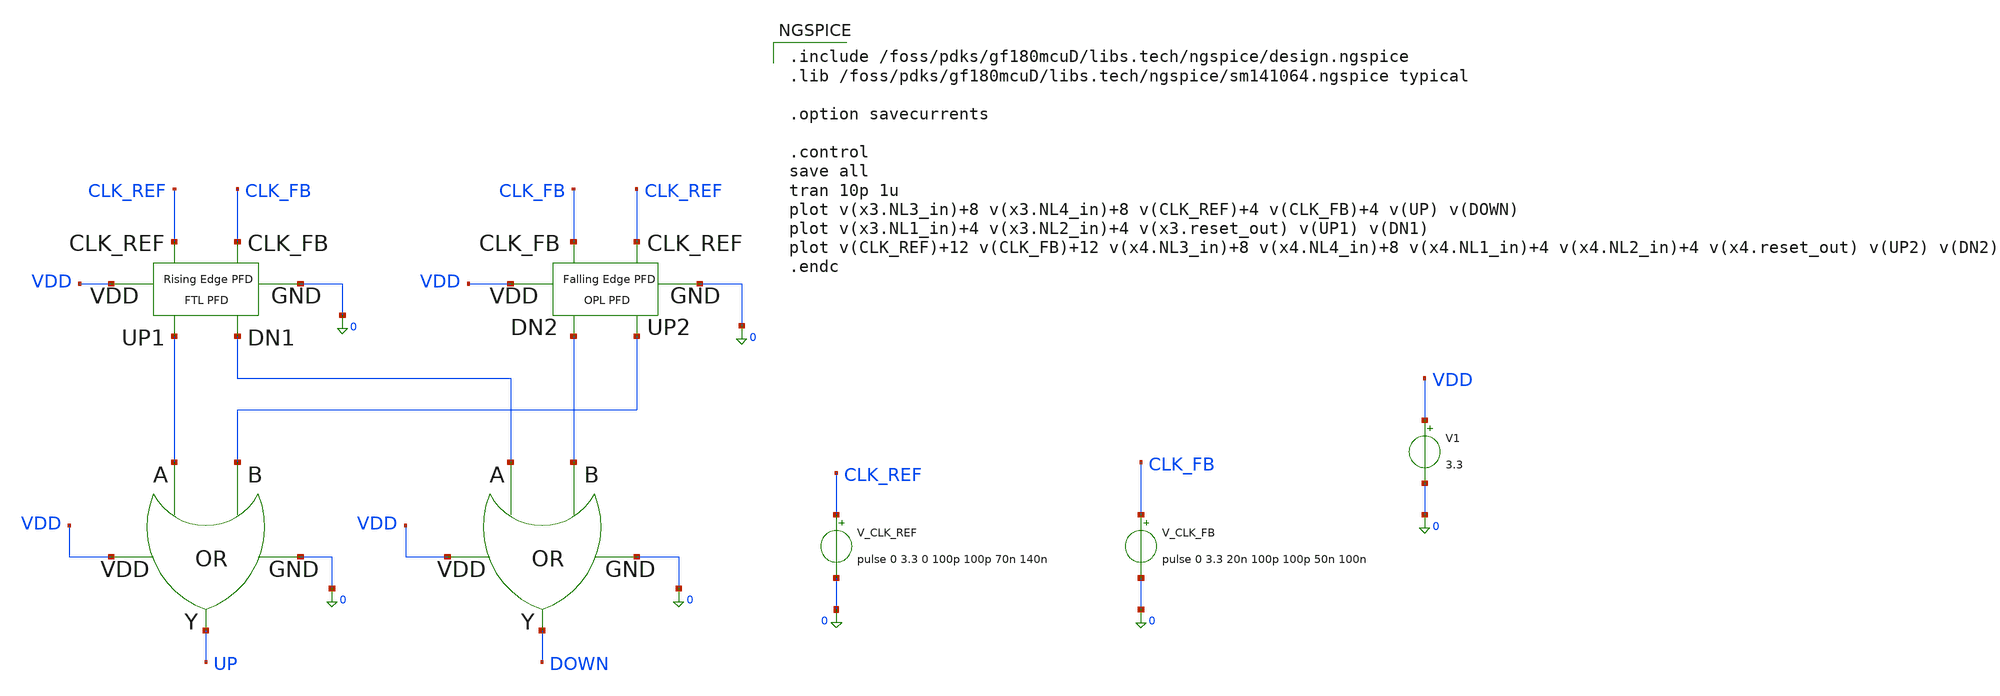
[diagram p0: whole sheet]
** sch_path: PFD/DELD_PFD.sch
**.subckt DELD_PFD
x1 0 DN1 DN2 VDD DOWN OR
x2 0 UP1 UP2 VDD UP OR
x3 DN1 UP1 CLK_FB CLK_REF VDD 0 FTL_PFD
x4 UP2 DN2 CLK_REF CLK_FB VDD 0 OPL_PFD
V1 VDD 0 3.3
.save i(v1)
V_CLK_REF CLK_REF 0 pulse 0 3.3 0 100p 100p 70n 140n
.save i(v_clk_ref)
V_CLK_FB CLK_FB 0 pulse 0 3.3 20n 100p 100p 50n 100n
.save i(v_clk_fb)
**** begin user architecture code

.include /foss/pdks/gf180mcuD/libs.tech/ngspice/design.ngspice
.lib /foss/pdks/gf180mcuD/libs.tech/ngspice/sm141064.ngspice typical

.option savecurrents

.control
save all
tran 10p 1u
plot v(x3.NL3_in)+8 v(x3.NL4_in)+8 v(CLK_REF)+4 v(CLK_FB)+4 v(UP) v(DOWN)
plot v(x3.NL1_in)+4 v(x3.NL2_in)+4 v(x3.reset_out) v(UP1) v(DN1)
plot v(CLK_REF)+12 v(CLK_FB)+12 v(x4.NL3_in)+8 v(x4.NL4_in)+8 v(x4.NL1_in)+4 v(x4.NL2_in)+4
+ v(x4.reset_out) v(UP2) v(DN2)
.endc

**** end user architecture code
**.ends

* expanding   symbol:  OR.sym # of pins=5
** sym_path: PFD/OR.sym
** sch_path: PFD/OR.sch
.subckt OR GND A B VDD Y
*.opin Y
*.ipin GND
*.ipin VDD
*.ipin A
*.ipin B
XM3 net2 A GND GND nfet_03v3 L=0.28u W=0.22u nf=1 ad='int((nf+1)/2) * W/nf * 0.18u' as='int((nf+2)/2) * W/nf * 0.18u'
+ pd='2*int((nf+1)/2) * (W/nf + 0.18u)' ps='2*int((nf+2)/2) * (W/nf + 0.18u)' nrd='0.18u / W' nrs='0.18u / W'
+ sa=0 sb=0 sd=0 m=1
XM2 net1 A net3 VDD pfet_03v3 L=0.28u W=0.22u nf=1 ad='int((nf+1)/2) * W/nf * 0.18u' as='int((nf+2)/2) * W/nf * 0.18u'
+ pd='2*int((nf+1)/2) * (W/nf + 0.18u)' ps='2*int((nf+2)/2) * (W/nf + 0.18u)' nrd='0.18u / W' nrs='0.18u / W'
+ sa=0 sb=0 sd=0 m=3
XM4 net2 B net1 net4 pfet_03v3 L=0.28u W=0.22u nf=1 ad='int((nf+1)/2) * W/nf * 0.18u' as='int((nf+2)/2) * W/nf * 0.18u'
+ pd='2*int((nf+1)/2) * (W/nf + 0.18u)' ps='2*int((nf+2)/2) * (W/nf + 0.18u)' nrd='0.18u / W' nrs='0.18u / W'
+ sa=0 sb=0 sd=0 m=3
XM1 net2 B GND GND nfet_03v3 L=0.28u W=0.22u nf=1 ad='int((nf+1)/2) * W/nf * 0.18u' as='int((nf+2)/2) * W/nf * 0.18u'
+ pd='2*int((nf+1)/2) * (W/nf + 0.18u)' ps='2*int((nf+2)/2) * (W/nf + 0.18u)' nrd='0.18u / W' nrs='0.18u / W'
+ sa=0 sb=0 sd=0 m=1
XM29 Y net2 VDD VDD pfet_03v3 L=0.28u W=0.22u nf=1 ad='int((nf+1)/2) * W/nf * 0.18u' as='int((nf+2)/2) * W/nf * 0.18u'
+ pd='2*int((nf+1)/2) * (W/nf + 0.18u)' ps='2*int((nf+2)/2) * (W/nf + 0.18u)' nrd='0.18u / W' nrs='0.18u / W'
+ sa=0 sb=0 sd=0 m=3
XM30 Y net2 GND GND nfet_03v3 L=0.28u W=0.22u nf=1 ad='int((nf+1)/2) * W/nf * 0.18u' as='int((nf+2)/2) * W/nf * 0.18u'
+ pd='2*int((nf+1)/2) * (W/nf + 0.18u)' ps='2*int((nf+2)/2) * (W/nf + 0.18u)' nrd='0.18u / W' nrs='0.18u / W'
+ sa=0 sb=0 sd=0 m=1
.ends


* expanding   symbol:  FTL_PFD.sym # of pins=6
** sym_path: PFD/FTL_PFD.sym
** sch_path: PFD/FTL_PFD.sch
.subckt FTL_PFD DN1 UP1 CLK_FB CLK_REF VDD GND
*.opin UP1
*.opin DN1
*.ipin CLK_FB
*.ipin CLK_REF
*.iopin VDD
*.iopin GND
XM1 net1 net3 VDD VDD pfet_03v3 L=0.28u W=0.22u nf=1 ad='int((nf+1)/2) * W/nf * 0.18u' as='int((nf+2)/2) * W/nf * 0.18u'
+ pd='2*int((nf+1)/2) * (W/nf + 0.18u)' ps='2*int((nf+2)/2) * (W/nf + 0.18u)' nrd='0.18u / W' nrs='0.18u / W'
+ sa=0 sb=0 sd=0 m=3
XM4 net2 net3 GND GND nfet_03v3 L=0.28u W=0.22u nf=1 ad='int((nf+1)/2) * W/nf * 0.18u' as='int((nf+2)/2) * W/nf * 0.18u'
+ pd='2*int((nf+1)/2) * (W/nf + 0.18u)' ps='2*int((nf+2)/2) * (W/nf + 0.18u)' nrd='0.18u / W' nrs='0.18u / W'
+ sa=0 sb=0 sd=0 m=1
XM2 net2 CLK_REF net1 VDD pfet_03v3 L=0.28u W=0.22u nf=1 ad='int((nf+1)/2) * W/nf * 0.18u' as='int((nf+2)/2) * W/nf * 0.18u'
+ pd='2*int((nf+1)/2) * (W/nf + 0.18u)' ps='2*int((nf+2)/2) * (W/nf + 0.18u)' nrd='0.18u / W' nrs='0.18u / W'
+ sa=0 sb=0 sd=0 m=3
XM3 net2 CLK_REF GND GND nfet_03v3 L=0.28u W=0.22u nf=1 ad='int((nf+1)/2) * W/nf * 0.18u' as='int((nf+2)/2) * W/nf * 0.18u'
+ pd='2*int((nf+1)/2) * (W/nf + 0.18u)' ps='2*int((nf+2)/2) * (W/nf + 0.18u)' nrd='0.18u / W' nrs='0.18u / W'
+ sa=0 sb=0 sd=0 m=1
XM5 net4 net2 VDD VDD pfet_03v3 L=0.28u W=0.22u nf=1 ad='int((nf+1)/2) * W/nf * 0.18u' as='int((nf+2)/2) * W/nf * 0.18u'
+ pd='2*int((nf+1)/2) * (W/nf + 0.18u)' ps='2*int((nf+2)/2) * (W/nf + 0.18u)' nrd='0.18u / W' nrs='0.18u / W'
+ sa=0 sb=0 sd=0 m=3
XM6 net5 CLK_REF net4 VDD pfet_03v3 L=0.28u W=0.22u nf=1 ad='int((nf+1)/2) * W/nf * 0.18u' as='int((nf+2)/2) * W/nf * 0.18u'
+ pd='2*int((nf+1)/2) * (W/nf + 0.18u)' ps='2*int((nf+2)/2) * (W/nf + 0.18u)' nrd='0.18u / W' nrs='0.18u / W'
+ sa=0 sb=0 sd=0 m=3
XM7 net5 net2 GND GND nfet_03v3 L=0.28u W=0.22u nf=1 ad='int((nf+1)/2) * W/nf * 0.18u' as='int((nf+2)/2) * W/nf * 0.18u'
+ pd='2*int((nf+1)/2) * (W/nf + 0.18u)' ps='2*int((nf+2)/2) * (W/nf + 0.18u)' nrd='0.18u / W' nrs='0.18u / W'
+ sa=0 sb=0 sd=0 m=1
XM9 net6 CLK_REF_bar VDD VDD pfet_03v3 L=0.28u W=0.22u nf=1 ad='int((nf+1)/2) * W/nf * 0.18u' as='int((nf+2)/2) * W/nf * 0.18u'
+ pd='2*int((nf+1)/2) * (W/nf + 0.18u)' ps='2*int((nf+2)/2) * (W/nf + 0.18u)' nrd='0.18u / W' nrs='0.18u / W'
+ sa=0 sb=0 sd=0 m=3
XM10 net7 net5 GND GND nfet_03v3 L=0.28u W=0.22u nf=1 ad='int((nf+1)/2) * W/nf * 0.18u' as='int((nf+2)/2) * W/nf * 0.18u'
+ pd='2*int((nf+1)/2) * (W/nf + 0.18u)' ps='2*int((nf+2)/2) * (W/nf + 0.18u)' nrd='0.18u / W' nrs='0.18u / W'
+ sa=0 sb=0 sd=0 m=1
XM8 net7 net5 net6 VDD pfet_03v3 L=0.28u W=0.22u nf=1 ad='int((nf+1)/2) * W/nf * 0.18u' as='int((nf+2)/2) * W/nf * 0.18u'
+ pd='2*int((nf+1)/2) * (W/nf + 0.18u)' ps='2*int((nf+2)/2) * (W/nf + 0.18u)' nrd='0.18u / W' nrs='0.18u / W'
+ sa=0 sb=0 sd=0 m=3
XM11 net7 CLK_REF_bar GND GND nfet_03v3 L=0.28u W=0.22u nf=1 ad='int((nf+1)/2) * W/nf * 0.18u' as='int((nf+2)/2) * W/nf * 0.18u'
+ pd='2*int((nf+1)/2) * (W/nf + 0.18u)' ps='2*int((nf+2)/2) * (W/nf + 0.18u)' nrd='0.18u / W' nrs='0.18u / W'
+ sa=0 sb=0 sd=0 m=1
XM12 net8 net7 VDD VDD pfet_03v3 L=0.28u W=0.22u nf=1 ad='int((nf+1)/2) * W/nf * 0.18u' as='int((nf+2)/2) * W/nf * 0.18u'
+ pd='2*int((nf+1)/2) * (W/nf + 0.18u)' ps='2*int((nf+2)/2) * (W/nf + 0.18u)' nrd='0.18u / W' nrs='0.18u / W'
+ sa=0 sb=0 sd=0 m=3
XM13 UP1 CLK_REF_bar net8 VDD pfet_03v3 L=0.28u W=0.22u nf=1 ad='int((nf+1)/2) * W/nf * 0.18u' as='int((nf+2)/2) * W/nf * 0.18u'
+ pd='2*int((nf+1)/2) * (W/nf + 0.18u)' ps='2*int((nf+2)/2) * (W/nf + 0.18u)' nrd='0.18u / W' nrs='0.18u / W'
+ sa=0 sb=0 sd=0 m=3
XM14 UP1 net7 GND GND nfet_03v3 L=0.28u W=0.22u nf=1 ad='int((nf+1)/2) * W/nf * 0.18u' as='int((nf+2)/2) * W/nf * 0.18u'
+ pd='2*int((nf+1)/2) * (W/nf + 0.18u)' ps='2*int((nf+2)/2) * (W/nf + 0.18u)' nrd='0.18u / W' nrs='0.18u / W'
+ sa=0 sb=0 sd=0 m=1
XM15 net9 net3 VDD VDD pfet_03v3 L=0.28u W=0.22u nf=1 ad='int((nf+1)/2) * W/nf * 0.18u' as='int((nf+2)/2) * W/nf * 0.18u'
+ pd='2*int((nf+1)/2) * (W/nf + 0.18u)' ps='2*int((nf+2)/2) * (W/nf + 0.18u)' nrd='0.18u / W' nrs='0.18u / W'
+ sa=0 sb=0 sd=0 m=3
XM16 net10 net3 GND GND nfet_03v3 L=0.28u W=0.22u nf=1 ad='int((nf+1)/2) * W/nf * 0.18u' as='int((nf+2)/2) * W/nf * 0.18u'
+ pd='2*int((nf+1)/2) * (W/nf + 0.18u)' ps='2*int((nf+2)/2) * (W/nf + 0.18u)' nrd='0.18u / W' nrs='0.18u / W'
+ sa=0 sb=0 sd=0 m=1
XM17 net10 CLK_FB net9 VDD pfet_03v3 L=0.28u W=0.22u nf=1 ad='int((nf+1)/2) * W/nf * 0.18u' as='int((nf+2)/2) * W/nf * 0.18u'
+ pd='2*int((nf+1)/2) * (W/nf + 0.18u)' ps='2*int((nf+2)/2) * (W/nf + 0.18u)' nrd='0.18u / W' nrs='0.18u / W'
+ sa=0 sb=0 sd=0 m=3
XM18 net10 CLK_FB GND GND nfet_03v3 L=0.28u W=0.22u nf=1 ad='int((nf+1)/2) * W/nf * 0.18u' as='int((nf+2)/2) * W/nf * 0.18u'
+ pd='2*int((nf+1)/2) * (W/nf + 0.18u)' ps='2*int((nf+2)/2) * (W/nf + 0.18u)' nrd='0.18u / W' nrs='0.18u / W'
+ sa=0 sb=0 sd=0 m=1
XM19 net11 net10 VDD VDD pfet_03v3 L=0.28u W=0.22u nf=1 ad='int((nf+1)/2) * W/nf * 0.18u' as='int((nf+2)/2) * W/nf * 0.18u'
+ pd='2*int((nf+1)/2) * (W/nf + 0.18u)' ps='2*int((nf+2)/2) * (W/nf + 0.18u)' nrd='0.18u / W' nrs='0.18u / W'
+ sa=0 sb=0 sd=0 m=3
XM20 net12 CLK_FB net11 VDD pfet_03v3 L=0.28u W=0.22u nf=1 ad='int((nf+1)/2) * W/nf * 0.18u' as='int((nf+2)/2) * W/nf * 0.18u'
+ pd='2*int((nf+1)/2) * (W/nf + 0.18u)' ps='2*int((nf+2)/2) * (W/nf + 0.18u)' nrd='0.18u / W' nrs='0.18u / W'
+ sa=0 sb=0 sd=0 m=3
XM21 net12 net10 GND GND nfet_03v3 L=0.28u W=0.22u nf=1 ad='int((nf+1)/2) * W/nf * 0.18u' as='int((nf+2)/2) * W/nf * 0.18u'
+ pd='2*int((nf+1)/2) * (W/nf + 0.18u)' ps='2*int((nf+2)/2) * (W/nf + 0.18u)' nrd='0.18u / W' nrs='0.18u / W'
+ sa=0 sb=0 sd=0 m=1
XM22 net13 CLK_FB_bar VDD VDD pfet_03v3 L=0.28u W=0.22u nf=1 ad='int((nf+1)/2) * W/nf * 0.18u' as='int((nf+2)/2) * W/nf * 0.18u'
+ pd='2*int((nf+1)/2) * (W/nf + 0.18u)' ps='2*int((nf+2)/2) * (W/nf + 0.18u)' nrd='0.18u / W' nrs='0.18u / W'
+ sa=0 sb=0 sd=0 m=3
XM23 net14 net12 GND GND nfet_03v3 L=0.28u W=0.22u nf=1 ad='int((nf+1)/2) * W/nf * 0.18u' as='int((nf+2)/2) * W/nf * 0.18u'
+ pd='2*int((nf+1)/2) * (W/nf + 0.18u)' ps='2*int((nf+2)/2) * (W/nf + 0.18u)' nrd='0.18u / W' nrs='0.18u / W'
+ sa=0 sb=0 sd=0 m=1
XM24 net14 net12 net13 VDD pfet_03v3 L=0.28u W=0.22u nf=1 ad='int((nf+1)/2) * W/nf * 0.18u' as='int((nf+2)/2) * W/nf * 0.18u'
+ pd='2*int((nf+1)/2) * (W/nf + 0.18u)' ps='2*int((nf+2)/2) * (W/nf + 0.18u)' nrd='0.18u / W' nrs='0.18u / W'
+ sa=0 sb=0 sd=0 m=3
XM25 net14 CLK_FB_bar GND GND nfet_03v3 L=0.28u W=0.22u nf=1 ad='int((nf+1)/2) * W/nf * 0.18u' as='int((nf+2)/2) * W/nf * 0.18u'
+ pd='2*int((nf+1)/2) * (W/nf + 0.18u)' ps='2*int((nf+2)/2) * (W/nf + 0.18u)' nrd='0.18u / W' nrs='0.18u / W'
+ sa=0 sb=0 sd=0 m=1
XM26 net15 net14 VDD VDD pfet_03v3 L=0.28u W=0.22u nf=1 ad='int((nf+1)/2) * W/nf * 0.18u' as='int((nf+2)/2) * W/nf * 0.18u'
+ pd='2*int((nf+1)/2) * (W/nf + 0.18u)' ps='2*int((nf+2)/2) * (W/nf + 0.18u)' nrd='0.18u / W' nrs='0.18u / W'
+ sa=0 sb=0 sd=0 m=3
XM27 DN1 CLK_FB_bar net15 VDD pfet_03v3 L=0.28u W=0.22u nf=1 ad='int((nf+1)/2) * W/nf * 0.18u' as='int((nf+2)/2) * W/nf * 0.18u'
+ pd='2*int((nf+1)/2) * (W/nf + 0.18u)' ps='2*int((nf+2)/2) * (W/nf + 0.18u)' nrd='0.18u / W' nrs='0.18u / W'
+ sa=0 sb=0 sd=0 m=3
XM28 DN1 net14 GND GND nfet_03v3 L=0.28u W=0.22u nf=1 ad='int((nf+1)/2) * W/nf * 0.18u' as='int((nf+2)/2) * W/nf * 0.18u'
+ pd='2*int((nf+1)/2) * (W/nf + 0.18u)' ps='2*int((nf+2)/2) * (W/nf + 0.18u)' nrd='0.18u / W' nrs='0.18u / W'
+ sa=0 sb=0 sd=0 m=1
x1 GND UP1 DN1 VDD net3 XNOR
XM29 CLK_FB_bar CLK_FB VDD VDD pfet_03v3 L=0.28u W=0.22u nf=1 ad='int((nf+1)/2) * W/nf * 0.18u' as='int((nf+2)/2) * W/nf * 0.18u'
+ pd='2*int((nf+1)/2) * (W/nf + 0.18u)' ps='2*int((nf+2)/2) * (W/nf + 0.18u)' nrd='0.18u / W' nrs='0.18u / W'
+ sa=0 sb=0 sd=0 m=3
XM30 CLK_FB_bar CLK_FB GND GND nfet_03v3 L=0.28u W=0.22u nf=1 ad='int((nf+1)/2) * W/nf * 0.18u' as='int((nf+2)/2) * W/nf * 0.18u'
+ pd='2*int((nf+1)/2) * (W/nf + 0.18u)' ps='2*int((nf+2)/2) * (W/nf + 0.18u)' nrd='0.18u / W' nrs='0.18u / W'
+ sa=0 sb=0 sd=0 m=1
XM31 CLK_REF_bar CLK_REF VDD VDD pfet_03v3 L=0.28u W=0.22u nf=1 ad='int((nf+1)/2) * W/nf * 0.18u' as='int((nf+2)/2) * W/nf * 0.18u'
+ pd='2*int((nf+1)/2) * (W/nf + 0.18u)' ps='2*int((nf+2)/2) * (W/nf + 0.18u)' nrd='0.18u / W' nrs='0.18u / W'
+ sa=0 sb=0 sd=0 m=3
XM32 CLK_REF_bar CLK_REF GND GND nfet_03v3 L=0.28u W=0.22u nf=1 ad='int((nf+1)/2) * W/nf * 0.18u' as='int((nf+2)/2) * W/nf * 0.18u'
+ pd='2*int((nf+1)/2) * (W/nf + 0.18u)' ps='2*int((nf+2)/2) * (W/nf + 0.18u)' nrd='0.18u / W' nrs='0.18u / W'
+ sa=0 sb=0 sd=0 m=1
.ends


* expanding   symbol:  OPL_PFD.sym # of pins=6
** sym_path: PFD/OPL_PFD.sym
** sch_path: PFD/OPL_PFD.sch
.subckt OPL_PFD UP2 DN2 CLK_REF CLK_FB VDD GND
*.opin UP2
*.ipin CLK_FB
*.ipin CLK_REF
*.opin DN2
*.iopin VDD
*.iopin GND
XM1 NL1_in reset_out VDD VDD pfet_03v3 L=0.28u W=0.22u nf=1 ad='int((nf+1)/2) * W/nf * 0.18u' as='int((nf+2)/2) * W/nf * 0.18u'
+ pd='2*int((nf+1)/2) * (W/nf + 0.18u)' ps='2*int((nf+2)/2) * (W/nf + 0.18u)' nrd='0.18u / W' nrs='0.18u / W'
+ sa=0 sb=0 sd=0 m=3
XM4 net1 reset_out GND GND nfet_03v3 L=0.28u W=0.22u nf=1 ad='int((nf+1)/2) * W/nf * 0.18u' as='int((nf+2)/2) * W/nf * 0.18u'
+ pd='2*int((nf+1)/2) * (W/nf + 0.18u)' ps='2*int((nf+2)/2) * (W/nf + 0.18u)' nrd='0.18u / W' nrs='0.18u / W'
+ sa=0 sb=0 sd=0 m=1
XM5 net2 NL1_in VDD VDD pfet_03v3 L=0.28u W=0.22u nf=1 ad='int((nf+1)/2) * W/nf * 0.18u' as='int((nf+2)/2) * W/nf * 0.18u'
+ pd='2*int((nf+1)/2) * (W/nf + 0.18u)' ps='2*int((nf+2)/2) * (W/nf + 0.18u)' nrd='0.18u / W' nrs='0.18u / W'
+ sa=0 sb=0 sd=0 m=3
XM7 net3 NL1_in GND GND nfet_03v3 L=0.28u W=0.22u nf=1 ad='int((nf+1)/2) * W/nf * 0.18u' as='int((nf+2)/2) * W/nf * 0.18u'
+ pd='2*int((nf+1)/2) * (W/nf + 0.18u)' ps='2*int((nf+2)/2) * (W/nf + 0.18u)' nrd='0.18u / W' nrs='0.18u / W'
+ sa=0 sb=0 sd=0 m=1
XM9 NL2_in CLK_REF_bar VDD VDD pfet_03v3 L=0.28u W=0.22u nf=1 ad='int((nf+1)/2) * W/nf * 0.18u' as='int((nf+2)/2) * W/nf * 0.18u'
+ pd='2*int((nf+1)/2) * (W/nf + 0.18u)' ps='2*int((nf+2)/2) * (W/nf + 0.18u)' nrd='0.18u / W' nrs='0.18u / W'
+ sa=0 sb=0 sd=0 m=3
XM11 net8 CLK_REF_bar GND GND nfet_03v3 L=0.28u W=0.22u nf=1 ad='int((nf+1)/2) * W/nf * 0.18u' as='int((nf+2)/2) * W/nf * 0.18u'
+ pd='2*int((nf+1)/2) * (W/nf + 0.18u)' ps='2*int((nf+2)/2) * (W/nf + 0.18u)' nrd='0.18u / W' nrs='0.18u / W'
+ sa=0 sb=0 sd=0 m=1
XM12 net7 NL2_in VDD VDD pfet_03v3 L=0.28u W=0.22u nf=1 ad='int((nf+1)/2) * W/nf * 0.18u' as='int((nf+2)/2) * W/nf * 0.18u'
+ pd='2*int((nf+1)/2) * (W/nf + 0.18u)' ps='2*int((nf+2)/2) * (W/nf + 0.18u)' nrd='0.18u / W' nrs='0.18u / W'
+ sa=0 sb=0 sd=0 m=1
XM14 net9 NL2_in GND GND nfet_03v3 L=0.28u W=0.22u nf=1 ad='int((nf+1)/2) * W/nf * 0.18u' as='int((nf+2)/2) * W/nf * 0.18u'
+ pd='2*int((nf+1)/2) * (W/nf + 0.18u)' ps='2*int((nf+2)/2) * (W/nf + 0.18u)' nrd='0.18u / W' nrs='0.18u / W'
+ sa=0 sb=0 sd=0 m=1
XM2 NL1_in CLK_REF VDD VDD pfet_03v3 L=0.28u W=0.22u nf=1 ad='int((nf+1)/2) * W/nf * 0.18u' as='int((nf+2)/2) * W/nf * 0.18u'
+ pd='2*int((nf+1)/2) * (W/nf + 0.18u)' ps='2*int((nf+2)/2) * (W/nf + 0.18u)' nrd='0.18u / W' nrs='0.18u / W'
+ sa=0 sb=0 sd=0 m=3
XM6 net2 CLK_REF net3 GND nfet_03v3 L=0.28u W=0.22u nf=1 ad='int((nf+1)/2) * W/nf * 0.18u' as='int((nf+2)/2) * W/nf * 0.18u'
+ pd='2*int((nf+1)/2) * (W/nf + 0.18u)' ps='2*int((nf+2)/2) * (W/nf + 0.18u)' nrd='0.18u / W' nrs='0.18u / W'
+ sa=0 sb=0 sd=0 m=1
XM10 NL2_in net2 net8 GND nfet_03v3 L=0.28u W=0.22u nf=1 ad='int((nf+1)/2) * W/nf * 0.18u' as='int((nf+2)/2) * W/nf * 0.18u'
+ pd='2*int((nf+1)/2) * (W/nf + 0.18u)' ps='2*int((nf+2)/2) * (W/nf + 0.18u)' nrd='0.18u / W' nrs='0.18u / W'
+ sa=0 sb=0 sd=0 m=1
XM8 NL2_in net2 VDD VDD pfet_03v3 L=0.28u W=0.22u nf=1 ad='int((nf+1)/2) * W/nf * 0.18u' as='int((nf+2)/2) * W/nf * 0.18u'
+ pd='2*int((nf+1)/2) * (W/nf + 0.18u)' ps='2*int((nf+2)/2) * (W/nf + 0.18u)' nrd='0.18u / W' nrs='0.18u / W'
+ sa=0 sb=0 sd=0 m=3
XM13 net7 CLK_REF_bar net9 GND nfet_03v3 L=0.28u W=0.22u nf=1 ad='int((nf+1)/2) * W/nf * 0.18u' as='int((nf+2)/2) * W/nf * 0.18u'
+ pd='2*int((nf+1)/2) * (W/nf + 0.18u)' ps='2*int((nf+2)/2) * (W/nf + 0.18u)' nrd='0.18u / W' nrs='0.18u / W'
+ sa=0 sb=0 sd=0 m=1
XM15 UP2 net7 VDD VDD pfet_03v3 L=0.28u W=0.22u nf=1 ad='int((nf+1)/2) * W/nf * 0.18u' as='int((nf+2)/2) * W/nf * 0.18u'
+ pd='2*int((nf+1)/2) * (W/nf + 0.18u)' ps='2*int((nf+2)/2) * (W/nf + 0.18u)' nrd='0.18u / W' nrs='0.18u / W'
+ sa=0 sb=0 sd=0 m=3
XM16 UP2 net7 GND GND nfet_03v3 L=0.28u W=0.22u nf=1 ad='int((nf+1)/2) * W/nf * 0.18u' as='int((nf+2)/2) * W/nf * 0.18u'
+ pd='2*int((nf+1)/2) * (W/nf + 0.18u)' ps='2*int((nf+2)/2) * (W/nf + 0.18u)' nrd='0.18u / W' nrs='0.18u / W'
+ sa=0 sb=0 sd=0 m=1
XM17 CLK_FB_bar CLK_FB VDD VDD pfet_03v3 L=0.28u W=0.22u nf=1 ad='int((nf+1)/2) * W/nf * 0.18u' as='int((nf+2)/2) * W/nf * 0.18u'
+ pd='2*int((nf+1)/2) * (W/nf + 0.18u)' ps='2*int((nf+2)/2) * (W/nf + 0.18u)' nrd='0.18u / W' nrs='0.18u / W'
+ sa=0 sb=0 sd=0 m=3
XM18 CLK_FB_bar CLK_FB GND GND nfet_03v3 L=0.28u W=0.22u nf=1 ad='int((nf+1)/2) * W/nf * 0.18u' as='int((nf+2)/2) * W/nf * 0.18u'
+ pd='2*int((nf+1)/2) * (W/nf + 0.18u)' ps='2*int((nf+2)/2) * (W/nf + 0.18u)' nrd='0.18u / W' nrs='0.18u / W'
+ sa=0 sb=0 sd=0 m=1
XM19 CLK_REF_bar CLK_REF VDD VDD pfet_03v3 L=0.28u W=0.22u nf=1 ad='int((nf+1)/2) * W/nf * 0.18u' as='int((nf+2)/2) * W/nf * 0.18u'
+ pd='2*int((nf+1)/2) * (W/nf + 0.18u)' ps='2*int((nf+2)/2) * (W/nf + 0.18u)' nrd='0.18u / W' nrs='0.18u / W'
+ sa=0 sb=0 sd=0 m=3
XM20 CLK_REF_bar CLK_REF GND GND nfet_03v3 L=0.28u W=0.22u nf=1 ad='int((nf+1)/2) * W/nf * 0.18u' as='int((nf+2)/2) * W/nf * 0.18u'
+ pd='2*int((nf+1)/2) * (W/nf + 0.18u)' ps='2*int((nf+2)/2) * (W/nf + 0.18u)' nrd='0.18u / W' nrs='0.18u / W'
+ sa=0 sb=0 sd=0 m=1
XM3 NL1_in CLK_REF net1 GND nfet_03v3 L=0.28u W=0.22u nf=1 ad='int((nf+1)/2) * W/nf * 0.18u' as='int((nf+2)/2) * W/nf * 0.18u'
+ pd='2*int((nf+1)/2) * (W/nf + 0.18u)' ps='2*int((nf+2)/2) * (W/nf + 0.18u)' nrd='0.18u / W' nrs='0.18u / W'
+ sa=0 sb=0 sd=0 m=1
XM21 NL3_in reset_out VDD VDD pfet_03v3 L=0.28u W=0.22u nf=1 ad='int((nf+1)/2) * W/nf * 0.18u' as='int((nf+2)/2) * W/nf * 0.18u'
+ pd='2*int((nf+1)/2) * (W/nf + 0.18u)' ps='2*int((nf+2)/2) * (W/nf + 0.18u)' nrd='0.18u / W' nrs='0.18u / W'
+ sa=0 sb=0 sd=0 m=3
XM22 net10 reset_out GND GND nfet_03v3 L=0.28u W=0.22u nf=1 ad='int((nf+1)/2) * W/nf * 0.18u' as='int((nf+2)/2) * W/nf * 0.18u'
+ pd='2*int((nf+1)/2) * (W/nf + 0.18u)' ps='2*int((nf+2)/2) * (W/nf + 0.18u)' nrd='0.18u / W' nrs='0.18u / W'
+ sa=0 sb=0 sd=0 m=1
XM23 net6 NL3_in VDD VDD pfet_03v3 L=0.28u W=0.22u nf=1 ad='int((nf+1)/2) * W/nf * 0.18u' as='int((nf+2)/2) * W/nf * 0.18u'
+ pd='2*int((nf+1)/2) * (W/nf + 0.18u)' ps='2*int((nf+2)/2) * (W/nf + 0.18u)' nrd='0.18u / W' nrs='0.18u / W'
+ sa=0 sb=0 sd=0 m=3
XM24 net11 NL3_in GND GND nfet_03v3 L=0.28u W=0.22u nf=1 ad='int((nf+1)/2) * W/nf * 0.18u' as='int((nf+2)/2) * W/nf * 0.18u'
+ pd='2*int((nf+1)/2) * (W/nf + 0.18u)' ps='2*int((nf+2)/2) * (W/nf + 0.18u)' nrd='0.18u / W' nrs='0.18u / W'
+ sa=0 sb=0 sd=0 m=1
XM25 NL4_in CLK_FB_bar VDD VDD pfet_03v3 L=0.28u W=0.22u nf=1 ad='int((nf+1)/2) * W/nf * 0.18u' as='int((nf+2)/2) * W/nf * 0.18u'
+ pd='2*int((nf+1)/2) * (W/nf + 0.18u)' ps='2*int((nf+2)/2) * (W/nf + 0.18u)' nrd='0.18u / W' nrs='0.18u / W'
+ sa=0 sb=0 sd=0 m=3
XM26 net4 CLK_FB_bar GND GND nfet_03v3 L=0.28u W=0.22u nf=1 ad='int((nf+1)/2) * W/nf * 0.18u' as='int((nf+2)/2) * W/nf * 0.18u'
+ pd='2*int((nf+1)/2) * (W/nf + 0.18u)' ps='2*int((nf+2)/2) * (W/nf + 0.18u)' nrd='0.18u / W' nrs='0.18u / W'
+ sa=0 sb=0 sd=0 m=1
XM27 net5 NL4_in VDD VDD pfet_03v3 L=0.28u W=0.22u nf=1 ad='int((nf+1)/2) * W/nf * 0.18u' as='int((nf+2)/2) * W/nf * 0.18u'
+ pd='2*int((nf+1)/2) * (W/nf + 0.18u)' ps='2*int((nf+2)/2) * (W/nf + 0.18u)' nrd='0.18u / W' nrs='0.18u / W'
+ sa=0 sb=0 sd=0 m=1
XM28 net12 NL4_in GND GND nfet_03v3 L=0.28u W=0.22u nf=1 ad='int((nf+1)/2) * W/nf * 0.18u' as='int((nf+2)/2) * W/nf * 0.18u'
+ pd='2*int((nf+1)/2) * (W/nf + 0.18u)' ps='2*int((nf+2)/2) * (W/nf + 0.18u)' nrd='0.18u / W' nrs='0.18u / W'
+ sa=0 sb=0 sd=0 m=1
XM29 NL3_in CLK_FB VDD VDD pfet_03v3 L=0.28u W=0.22u nf=1 ad='int((nf+1)/2) * W/nf * 0.18u' as='int((nf+2)/2) * W/nf * 0.18u'
+ pd='2*int((nf+1)/2) * (W/nf + 0.18u)' ps='2*int((nf+2)/2) * (W/nf + 0.18u)' nrd='0.18u / W' nrs='0.18u / W'
+ sa=0 sb=0 sd=0 m=3
XM30 net6 CLK_FB net11 GND nfet_03v3 L=0.28u W=0.22u nf=1 ad='int((nf+1)/2) * W/nf * 0.18u' as='int((nf+2)/2) * W/nf * 0.18u'
+ pd='2*int((nf+1)/2) * (W/nf + 0.18u)' ps='2*int((nf+2)/2) * (W/nf + 0.18u)' nrd='0.18u / W' nrs='0.18u / W'
+ sa=0 sb=0 sd=0 m=1
XM31 NL4_in net6 net4 GND nfet_03v3 L=0.28u W=0.22u nf=1 ad='int((nf+1)/2) * W/nf * 0.18u' as='int((nf+2)/2) * W/nf * 0.18u'
+ pd='2*int((nf+1)/2) * (W/nf + 0.18u)' ps='2*int((nf+2)/2) * (W/nf + 0.18u)' nrd='0.18u / W' nrs='0.18u / W'
+ sa=0 sb=0 sd=0 m=1
XM32 NL4_in net6 VDD VDD pfet_03v3 L=0.28u W=0.22u nf=1 ad='int((nf+1)/2) * W/nf * 0.18u' as='int((nf+2)/2) * W/nf * 0.18u'
+ pd='2*int((nf+1)/2) * (W/nf + 0.18u)' ps='2*int((nf+2)/2) * (W/nf + 0.18u)' nrd='0.18u / W' nrs='0.18u / W'
+ sa=0 sb=0 sd=0 m=3
XM33 net5 CLK_FB_bar net12 GND nfet_03v3 L=0.28u W=0.22u nf=1 ad='int((nf+1)/2) * W/nf * 0.18u' as='int((nf+2)/2) * W/nf * 0.18u'
+ pd='2*int((nf+1)/2) * (W/nf + 0.18u)' ps='2*int((nf+2)/2) * (W/nf + 0.18u)' nrd='0.18u / W' nrs='0.18u / W'
+ sa=0 sb=0 sd=0 m=1
XM34 DN2 net5 VDD VDD pfet_03v3 L=0.28u W=0.22u nf=1 ad='int((nf+1)/2) * W/nf * 0.18u' as='int((nf+2)/2) * W/nf * 0.18u'
+ pd='2*int((nf+1)/2) * (W/nf + 0.18u)' ps='2*int((nf+2)/2) * (W/nf + 0.18u)' nrd='0.18u / W' nrs='0.18u / W'
+ sa=0 sb=0 sd=0 m=3
XM35 DN2 net5 GND GND nfet_03v3 L=0.28u W=0.22u nf=1 ad='int((nf+1)/2) * W/nf * 0.18u' as='int((nf+2)/2) * W/nf * 0.18u'
+ pd='2*int((nf+1)/2) * (W/nf + 0.18u)' ps='2*int((nf+2)/2) * (W/nf + 0.18u)' nrd='0.18u / W' nrs='0.18u / W'
+ sa=0 sb=0 sd=0 m=1
XM36 NL3_in CLK_FB net10 GND nfet_03v3 L=0.28u W=0.22u nf=1 ad='int((nf+1)/2) * W/nf * 0.18u' as='int((nf+2)/2) * W/nf * 0.18u'
+ pd='2*int((nf+1)/2) * (W/nf + 0.18u)' ps='2*int((nf+2)/2) * (W/nf + 0.18u)' nrd='0.18u / W' nrs='0.18u / W'
+ sa=0 sb=0 sd=0 m=1
x1 GND UP2 DN2 VDD reset_out NAND
.ends


* expanding   symbol:  XNOR.sym # of pins=5
** sym_path: PFD/XNOR.sym
** sch_path: PFD/XNOR.sch
.subckt XNOR GND A B VDD Y
*.opin Y
*.ipin A
*.ipin B
*.iopin VDD
*.iopin GND
XM1 net1 A VDD VDD pfet_03v3 L=0.28u W=0.22u nf=1 ad='int((nf+1)/2) * W/nf * 0.18u' as='int((nf+2)/2) * W/nf * 0.18u'
+ pd='2*int((nf+1)/2) * (W/nf + 0.18u)' ps='2*int((nf+2)/2) * (W/nf + 0.18u)' nrd='0.18u / W' nrs='0.18u / W'
+ sa=0 sb=0 sd=0 m=1
XM2 Y A_bar net1 VDD pfet_03v3 L=0.28u W=0.22u nf=1 ad='int((nf+1)/2) * W/nf * 0.18u' as='int((nf+2)/2) * W/nf * 0.18u'
+ pd='2*int((nf+1)/2) * (W/nf + 0.18u)' ps='2*int((nf+2)/2) * (W/nf + 0.18u)' nrd='0.18u / W' nrs='0.18u / W'
+ sa=0 sb=0 sd=0 m=1
XM3 Y B_bar net2 GND nfet_03v3 L=0.28u W=0.22u nf=1 ad='int((nf+1)/2) * W/nf * 0.18u' as='int((nf+2)/2) * W/nf * 0.18u'
+ pd='2*int((nf+1)/2) * (W/nf + 0.18u)' ps='2*int((nf+2)/2) * (W/nf + 0.18u)' nrd='0.18u / W' nrs='0.18u / W'
+ sa=0 sb=0 sd=0 m=1
XM4 net2 A GND GND nfet_03v3 L=0.28u W=0.22u nf=1 ad='int((nf+1)/2) * W/nf * 0.18u' as='int((nf+2)/2) * W/nf * 0.18u'
+ pd='2*int((nf+1)/2) * (W/nf + 0.18u)' ps='2*int((nf+2)/2) * (W/nf + 0.18u)' nrd='0.18u / W' nrs='0.18u / W'
+ sa=0 sb=0 sd=0 m=1
XM5 net3 B_bar VDD VDD pfet_03v3 L=0.28u W=0.22u nf=1 ad='int((nf+1)/2) * W/nf * 0.18u' as='int((nf+2)/2) * W/nf * 0.18u'
+ pd='2*int((nf+1)/2) * (W/nf + 0.18u)' ps='2*int((nf+2)/2) * (W/nf + 0.18u)' nrd='0.18u / W' nrs='0.18u / W'
+ sa=0 sb=0 sd=0 m=1
XM6 Y B net3 VDD pfet_03v3 L=0.28u W=0.22u nf=1 ad='int((nf+1)/2) * W/nf * 0.18u' as='int((nf+2)/2) * W/nf * 0.18u'
+ pd='2*int((nf+1)/2) * (W/nf + 0.18u)' ps='2*int((nf+2)/2) * (W/nf + 0.18u)' nrd='0.18u / W' nrs='0.18u / W'
+ sa=0 sb=0 sd=0 m=1
XM7 Y A_bar net4 GND nfet_03v3 L=0.28u W=0.22u nf=1 ad='int((nf+1)/2) * W/nf * 0.18u' as='int((nf+2)/2) * W/nf * 0.18u'
+ pd='2*int((nf+1)/2) * (W/nf + 0.18u)' ps='2*int((nf+2)/2) * (W/nf + 0.18u)' nrd='0.18u / W' nrs='0.18u / W'
+ sa=0 sb=0 sd=0 m=1
XM8 net4 B GND GND nfet_03v3 L=0.28u W=0.22u nf=1 ad='int((nf+1)/2) * W/nf * 0.18u' as='int((nf+2)/2) * W/nf * 0.18u'
+ pd='2*int((nf+1)/2) * (W/nf + 0.18u)' ps='2*int((nf+2)/2) * (W/nf + 0.18u)' nrd='0.18u / W' nrs='0.18u / W'
+ sa=0 sb=0 sd=0 m=1
XM9 A_bar A VDD VDD pfet_03v3 L=0.28u W=0.22u nf=1 ad='int((nf+1)/2) * W/nf * 0.18u' as='int((nf+2)/2) * W/nf * 0.18u'
+ pd='2*int((nf+1)/2) * (W/nf + 0.18u)' ps='2*int((nf+2)/2) * (W/nf + 0.18u)' nrd='0.18u / W' nrs='0.18u / W'
+ sa=0 sb=0 sd=0 m=3
XM10 A_bar A GND GND nfet_03v3 L=0.28u W=0.22u nf=1 ad='int((nf+1)/2) * W/nf * 0.18u' as='int((nf+2)/2) * W/nf * 0.18u'
+ pd='2*int((nf+1)/2) * (W/nf + 0.18u)' ps='2*int((nf+2)/2) * (W/nf + 0.18u)' nrd='0.18u / W' nrs='0.18u / W'
+ sa=0 sb=0 sd=0 m=1
XM11 B_bar B VDD VDD pfet_03v3 L=0.28u W=0.22u nf=1 ad='int((nf+1)/2) * W/nf * 0.18u' as='int((nf+2)/2) * W/nf * 0.18u'
+ pd='2*int((nf+1)/2) * (W/nf + 0.18u)' ps='2*int((nf+2)/2) * (W/nf + 0.18u)' nrd='0.18u / W' nrs='0.18u / W'
+ sa=0 sb=0 sd=0 m=3
XM12 B_bar B GND GND nfet_03v3 L=0.28u W=0.22u nf=1 ad='int((nf+1)/2) * W/nf * 0.18u' as='int((nf+2)/2) * W/nf * 0.18u'
+ pd='2*int((nf+1)/2) * (W/nf + 0.18u)' ps='2*int((nf+2)/2) * (W/nf + 0.18u)' nrd='0.18u / W' nrs='0.18u / W'
+ sa=0 sb=0 sd=0 m=1
.ends


* expanding   symbol:  NAND.sym # of pins=5
** sym_path: PFD/NAND.sym
** sch_path: PFD/NAND.sch
.subckt NAND GND A B VDD Y
*.opin Y
*.ipin GND
*.ipin VDD
*.ipin A
*.ipin B
XM1 Y A VDD VDD pfet_03v3 L=0.28u W=0.22u nf=1 ad='int((nf+1)/2) * W/nf * 0.18u' as='int((nf+2)/2) * W/nf * 0.18u'
+ pd='2*int((nf+1)/2) * (W/nf + 0.18u)' ps='2*int((nf+2)/2) * (W/nf + 0.18u)' nrd='0.18u / W' nrs='0.18u / W'
+ sa=0 sb=0 sd=0 m=3
XM3 Y A net1 GND nfet_03v3 L=0.28u W=0.22u nf=1 ad='int((nf+1)/2) * W/nf * 0.18u' as='int((nf+2)/2) * W/nf * 0.18u'
+ pd='2*int((nf+1)/2) * (W/nf + 0.18u)' ps='2*int((nf+2)/2) * (W/nf + 0.18u)' nrd='0.18u / W' nrs='0.18u / W'
+ sa=0 sb=0 sd=0 m=1
XM4 net1 B GND GND nfet_03v3 L=0.28u W=0.22u nf=1 ad='int((nf+1)/2) * W/nf * 0.18u' as='int((nf+2)/2) * W/nf * 0.18u'
+ pd='2*int((nf+1)/2) * (W/nf + 0.18u)' ps='2*int((nf+2)/2) * (W/nf + 0.18u)' nrd='0.18u / W' nrs='0.18u / W'
+ sa=0 sb=0 sd=0 m=1
XM2 Y B VDD VDD pfet_03v3 L=0.28u W=0.22u nf=1 ad='int((nf+1)/2) * W/nf * 0.18u' as='int((nf+2)/2) * W/nf * 0.18u'
+ pd='2*int((nf+1)/2) * (W/nf + 0.18u)' ps='2*int((nf+2)/2) * (W/nf + 0.18u)' nrd='0.18u / W' nrs='0.18u / W'
+ sa=0 sb=0 sd=0 m=3
.ends

.end
